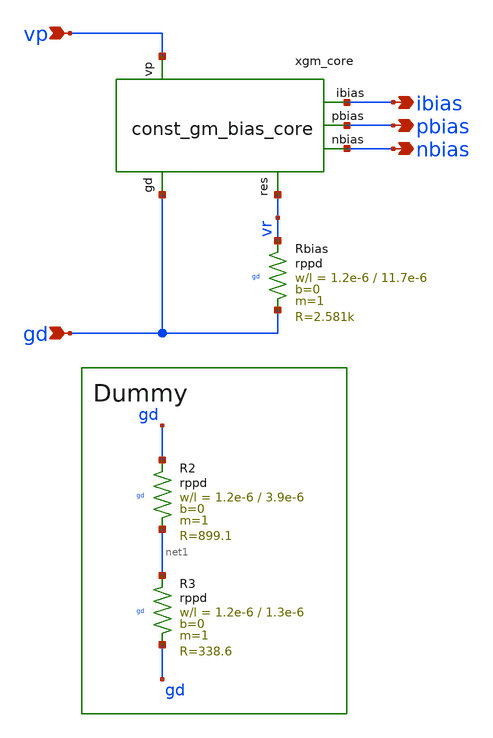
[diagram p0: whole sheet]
** sch_path: PLL0663-main/schematic/xschem/bandgap/const_gm_bias.sch
**.subckt const_gm_bias ibias vp gd pbias nbias
*.opin ibias
*.ipin vp
*.ipin gd
*.opin pbias
*.opin nbias
xgm_core vp ibias gd vr pbias nbias const_gm_bias_core
XRbias vr gd gd rppd w=1.2e-6 l=11.7e-6 m=1 b=0 mm_ok=1
XR2 gd net1 gd rppd w=1.2e-6 l=3.9e-6 m=1 b=0 mm_ok=1
XR3 net1 gd gd rppd w=1.2e-6 l=1.3e-6 m=1 b=0 mm_ok=1
**.ends
.end
